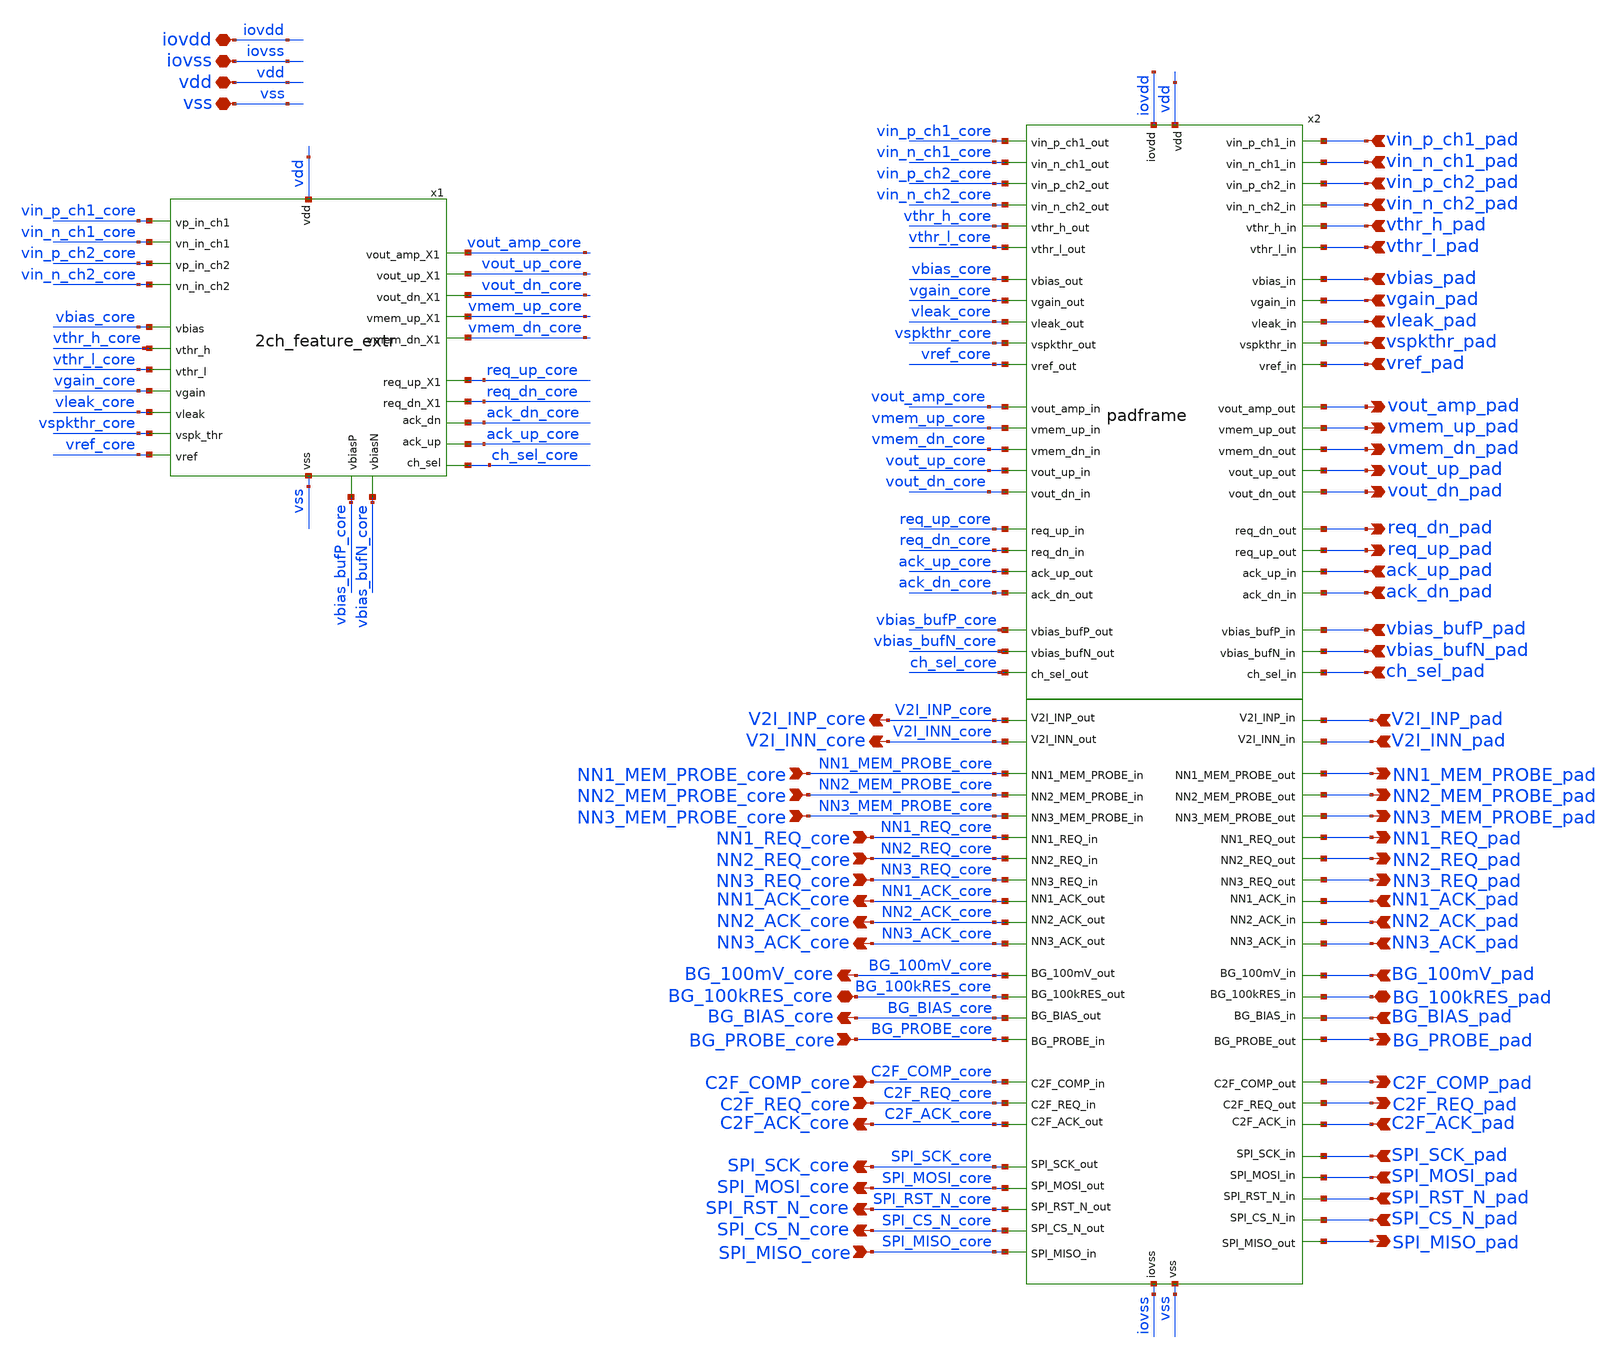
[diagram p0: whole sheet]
** sch_path: v2_feature_extr/top_FE.sch
**.subckt top_FE vin_p_ch1_pad vin_n_ch1_pad vin_p_ch2_pad vin_n_ch2_pad vthr_h_pad vthr_l_pad
*+ vbias_pad vgain_pad vleak_pad vspkthr_pad vref_pad vout_amp_pad vmem_up_pad vmem_dn_pad vout_up_pad
*+ vout_dn_pad req_dn_pad req_up_pad ack_up_pad ack_dn_pad vbias_bufP_pad vbias_bufN_pad ch_sel_pad iovdd iovss
*+ vdd vss V2I_INP_pad V2I_INN_pad NN1_ACK_pad NN2_ACK_pad NN3_ACK_pad BG_100mV_pad BG_100kRES_pad
*+ BG_BIAS_pad C2F_ACK_pad SPI_SCK_pad SPI_MOSI_pad SPI_RST_N_pad SPI_CS_N_pad NN1_MEM_PROBE_pad NN2_MEM_PROBE_pad
*+ NN3_MEM_PROBE_pad NN1_REQ_pad NN2_REQ_pad NN3_REQ_pad BG_PROBE_pad C2F_COMP_pad C2F_REQ_pad SPI_MISO_pad V2I_INP_core
*+ V2I_INN_core NN1_ACK_core NN2_ACK_core NN3_ACK_core BG_100mV_core BG_100kRES_core BG_BIAS_core C2F_ACK_core
*+ SPI_SCK_core SPI_MOSI_core SPI_RST_N_core SPI_CS_N_core NN1_MEM_PROBE_core NN2_MEM_PROBE_core NN3_MEM_PROBE_core
*+ NN1_REQ_core NN2_REQ_core NN3_REQ_core BG_PROBE_core C2F_COMP_core C2F_REQ_core SPI_MISO_core
*.ipin vin_p_ch1_pad
*.ipin vin_n_ch1_pad
*.ipin vin_p_ch2_pad
*.ipin vin_n_ch2_pad
*.ipin vthr_h_pad
*.ipin vthr_l_pad
*.ipin vbias_pad
*.ipin vgain_pad
*.ipin vleak_pad
*.ipin vspkthr_pad
*.ipin vref_pad
*.opin vout_amp_pad
*.opin vmem_up_pad
*.opin vmem_dn_pad
*.opin vout_up_pad
*.opin vout_dn_pad
*.opin req_dn_pad
*.opin req_up_pad
*.ipin ack_up_pad
*.ipin ack_dn_pad
*.ipin vbias_bufP_pad
*.ipin vbias_bufN_pad
*.ipin ch_sel_pad
*.iopin iovdd
*.iopin iovss
*.iopin vdd
*.iopin vss
*.ipin V2I_INP_pad
*.ipin V2I_INN_pad
*.ipin NN1_ACK_pad
*.ipin NN2_ACK_pad
*.ipin NN3_ACK_pad
*.ipin BG_100mV_pad
*.iopin BG_100kRES_pad
*.ipin BG_BIAS_pad
*.ipin C2F_ACK_pad
*.ipin SPI_SCK_pad
*.ipin SPI_MOSI_pad
*.ipin SPI_RST_N_pad
*.ipin SPI_CS_N_pad
*.opin NN1_MEM_PROBE_pad
*.opin NN2_MEM_PROBE_pad
*.opin NN3_MEM_PROBE_pad
*.opin NN1_REQ_pad
*.opin NN2_REQ_pad
*.opin NN3_REQ_pad
*.opin BG_PROBE_pad
*.opin C2F_COMP_pad
*.opin C2F_REQ_pad
*.opin SPI_MISO_pad
*.opin V2I_INP_core
*.opin V2I_INN_core
*.opin NN1_ACK_core
*.opin NN2_ACK_core
*.opin NN3_ACK_core
*.opin BG_100mV_core
*.iopin BG_100kRES_core
*.opin BG_BIAS_core
*.opin C2F_ACK_core
*.opin SPI_SCK_core
*.opin SPI_MOSI_core
*.opin SPI_RST_N_core
*.opin SPI_CS_N_core
*.ipin NN1_MEM_PROBE_core
*.ipin NN2_MEM_PROBE_core
*.ipin NN3_MEM_PROBE_core
*.ipin NN1_REQ_core
*.ipin NN2_REQ_core
*.ipin NN3_REQ_core
*.ipin BG_PROBE_core
*.ipin C2F_COMP_core
*.ipin C2F_REQ_core
*.ipin SPI_MISO_core
x1 vbias_core vdd vbias_bufP_core vss vbias_bufN_core vgain_core vleak_core vspkthr_core vref_core
+ vthr_h_core vin_p_ch1_core ack_up_core ack_dn_core vin_n_ch1_core vthr_l_core ch_sel_core vout_up_core
+ vmem_dn_core vmem_up_core vout_dn_core vin_p_ch2_core vin_n_ch2_core vout_amp_core req_up_core req_dn_core
+ 2ch_feature_extr
x2 SPI_CS_N_core SPI_CS_N_pad SPI_MISO_pad SPI_MISO_core SPI_SCK_core SPI_SCK_pad SPI_MOSI_core
+ SPI_MOSI_pad SPI_RST_N_core SPI_RST_N_pad C2F_REQ_pad C2F_REQ_core C2F_ACK_core C2F_ACK_pad C2F_COMP_pad
+ C2F_COMP_core NN1_REQ_pad NN1_REQ_core NN1_ACK_core NN1_ACK_pad NN2_REQ_pad NN2_REQ_core NN2_ACK_core NN2_ACK_pad
+ V2I_INN_core V2I_INP_core NN3_REQ_core BG_PROBE_core NN1_MEM_PROBE_core NN2_MEM_PROBE_core NN3_MEM_PROBE_core
+ NN3_ACK_core BG_BIAS_core BG_100kRES_core BG_100mV_core NN3_ACK_pad BG_100kRES_pad BG_BIAS_pad BG_100mV_pad
+ V2I_INN_pad NN3_REQ_pad BG_PROBE_pad NN1_MEM_PROBE_pad NN2_MEM_PROBE_pad NN3_MEM_PROBE_pad V2I_INP_pad
+ vbias_pad vspkthr_pad vref_pad vout_amp_pad vbias_bufP_pad vout_dn_pad vmem_dn_pad vleak_pad vbias_bufN_pad
+ vmem_up_pad vout_up_pad ch_sel_pad req_dn_pad req_up_pad vgain_pad iovss iovdd vdd vss ch_sel_core
+ vbias_bufN_core vref_core vbias_core vspkthr_core req_dn_core req_up_core vmem_dn_core vout_dn_core vbias_bufP_core
+ vleak_core vout_up_core vgain_core vout_amp_core vmem_up_core vin_p_ch1_core vin_p_ch1_pad ack_up_core
+ vin_n_ch1_core ack_up_pad vin_n_ch1_pad ack_dn_core vin_p_ch2_core ack_dn_pad vin_p_ch2_pad vin_n_ch2_core
+ vin_n_ch2_pad vthr_h_core vthr_h_pad vthr_l_core vthr_l_pad padframe
**.ends
.end
